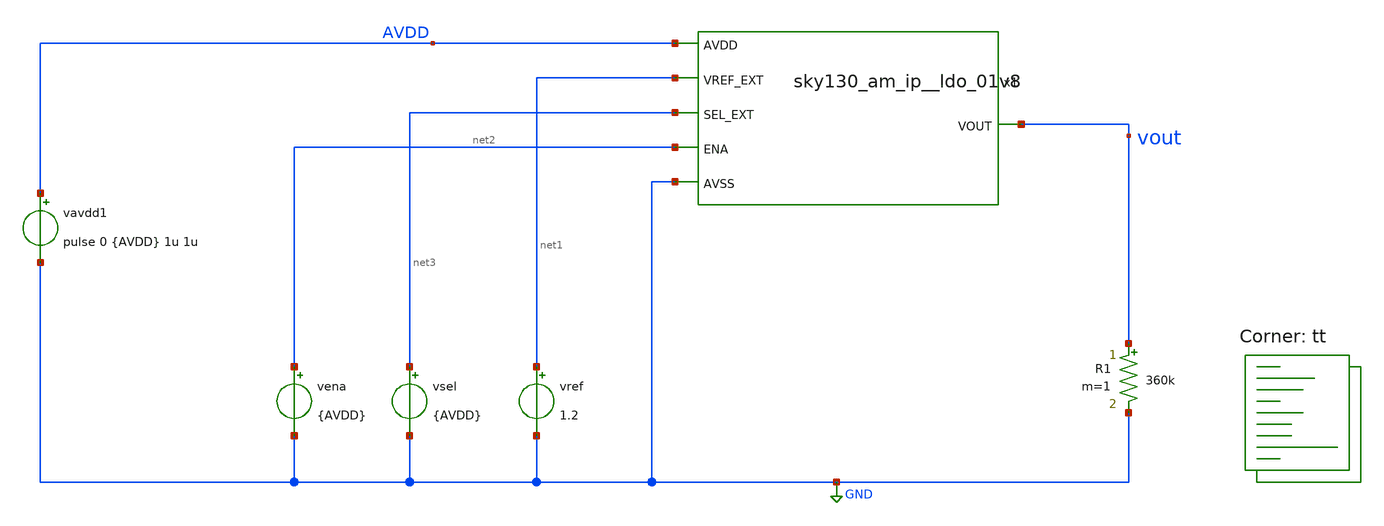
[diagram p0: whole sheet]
** sch_path: xschem/sky130_am_ip__ldo_01v8_tb.sch
**.subckt sky130_am_ip__ldo_01v8_tb
x1 AVDD vout GND net2 net1 net3 sky130_am_ip__ldo_01v8
R1 vout GND 360k m=1
vena net2 GND {AVDD}
vref net1 GND 1.2
vsel net3 GND {AVDD}
vavdd1 AVDD GND pulse 0 {AVDD} 1u 1u
**** begin user architecture code

.option savecurrents
.param AVDD = 3.3
.tran 100n 100u
.save all


.lib $::SKYWATER_MODELS/sky130.lib.spice tt


.include /home/efabless/.volare/sky130A/libs.ref/sky130_fd_sc_hvl/spice/sky130_fd_sc_hvl.spice




**** end user architecture code
**.ends
.GLOBAL GND
.end
